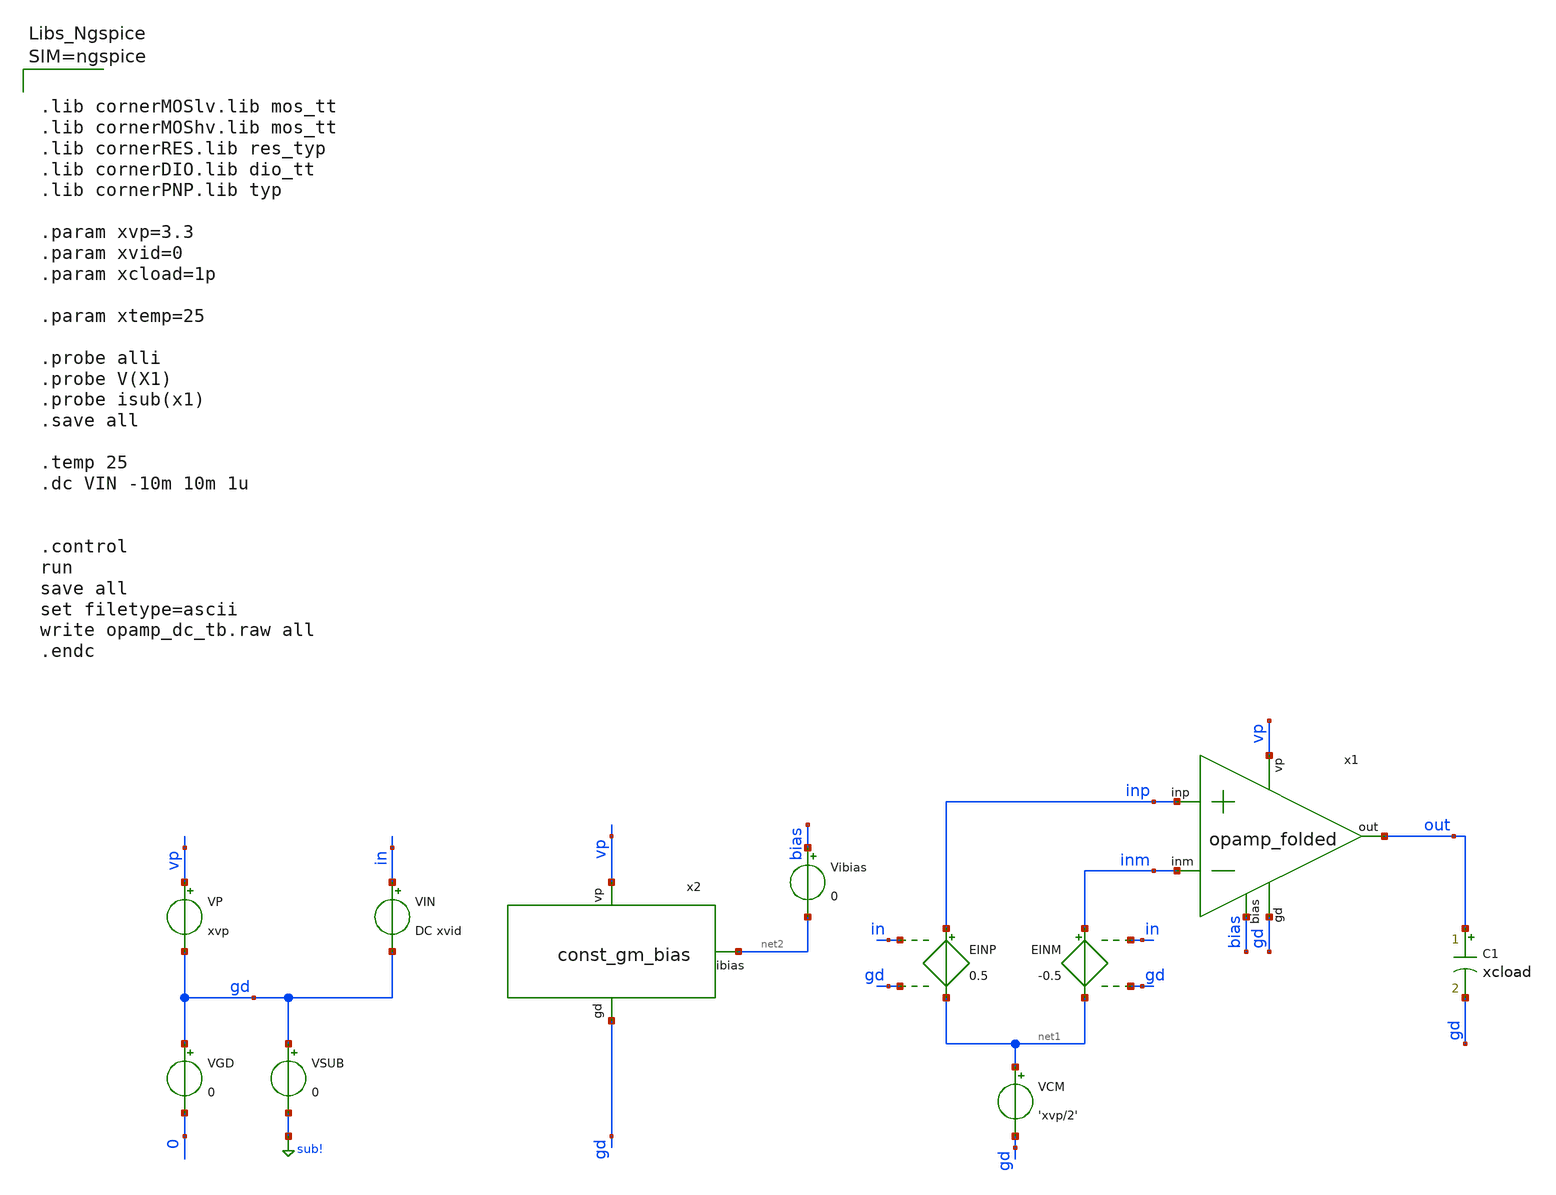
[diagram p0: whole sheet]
** sch_path: bandgap_res_tb/opamp_dc_tb.sch
**.subckt opamp_dc_tb
EINP inp net1 in gd 0.5
EINM inm net1 in gd -0.5
C1 out gd xcload m=1
VGD gd 0 0
VP vp gd xvp
VSUB gd sub! 0
VIN in gd DC xvid
VCM net1 gd 'xvp/2'
Vibias bias net2 0
.save i(vibias)
x1 vp inp inm out bias gd opamp_folded
x2 vp net2 gd const_gm_bias
**** begin user architecture code



.lib cornerMOSlv.lib mos_tt
.lib cornerMOShv.lib mos_tt
.lib cornerRES.lib res_typ
.lib cornerDIO.lib dio_tt
.lib cornerPNP.lib typ

.param xvp=3.3
.param xvid=0
.param xcload=1p

.param xtemp=25

.probe alli
.probe V(X1)
.probe isub(x1)
.save all

.temp 25
.dc VIN -10m 10m 1u


.control
run
save all
set filetype=ascii
write opamp_dc_tb.raw all
.endc



**** end user architecture code
**.ends

* expanding   symbol:  /foss/designs/master/bandgap_res/opamp_folded.sym # of pins=6
** sym_path: /foss/designs/master/bandgap_res/opamp_folded.sym
** sch_path: /foss/designs/master/bandgap_res/opamp_folded.sch
.subckt opamp_folded vp inp inm out bias gd
*.ipin bias
*.opin out
*.ipin vp
*.ipin inp
*.ipin inm
*.ipin gd
XM1 inp_fold inp net1 gd sg13_hv_nmos w=1.2u l=0.9u ng=1 m=4 mm_ok=1
XM2 inm_fold inm net1 gd sg13_hv_nmos w=1.2u l=0.9u ng=1 m=4 mm_ok=1
XM3 tele_p tele_g gd gd sg13_hv_nmos w=1.2u l=0.9u ng=1 m=2 mm_ok=1
XM4 tele_m tele_g gd gd sg13_hv_nmos w=1.2u l=0.9u ng=1 m=2 mm_ok=1
XM5 tele_g bias2 tele_p gd sg13_hv_nmos w=1.2u l=0.9u ng=1 m=2 mm_ok=1
XM6 out bias2 tele_m gd sg13_hv_nmos w=1.2u l=0.9u ng=1 m=2 mm_ok=1
XM7 tele_g bias3 inp_fold vp sg13_hv_pmos w=3.6u l=0.9u ng=1 m=2 mm_ok=1
XM8 out bias3 inm_fold vp sg13_hv_pmos w=3.6u l=0.9u ng=1 m=2 mm_ok=1
XM9 inp_fold bias4 vp vp sg13_hv_pmos w=3.6u l=0.9u ng=1 m=4 mm_ok=1
XM10 inm_fold bias4 vp vp sg13_hv_pmos w=3.6u l=0.9u ng=1 m=4 mm_ok=1
XM11 net1 bias gd gd sg13_hv_nmos w=1.2u l=0.9u ng=1 m=4 mm_ok=1
XM12 bias bias gd gd sg13_hv_nmos w=1.2u l=0.9u ng=1 m=2 mm_ok=1
XM13 bias4 bias gd gd sg13_hv_nmos w=1.2u l=0.9u ng=1 m=2 mm_ok=1
XM14 bias4 bias4 vp vp sg13_hv_pmos w=3.6u l=0.9u ng=1 m=2 mm_ok=1
XM15 bias3 bias gd gd sg13_hv_nmos w=1.2u l=0.9u ng=1 m=2 mm_ok=1
XM16 bias3 bias3 net3 vp sg13_hv_pmos w=3.6u l=0.9u ng=1 m=1 mm_ok=1
XM17 net3 bias3 vp vp sg13_hv_pmos w=3.6u l=0.9u ng=1 m=1 mm_ok=1
XM18 net2 bias2 gd gd sg13_hv_nmos w=1.2u l=0.9u ng=1 m=1 mm_ok=1
XM19 bias2 bias2 net2 gd sg13_hv_nmos w=1.2u l=0.9u ng=1 m=1 mm_ok=1
XM20 bias2 bias4 vp vp sg13_hv_pmos w=3.6u l=0.9u ng=1 m=4 mm_ok=1
.ends


* expanding   symbol:  /foss/designs/master/bandgap_res/const_gm_bias.sym # of pins=3
** sym_path: bandgap_res/const_gm_bias.sym
** sch_path: bandgap_res/const_gm_bias.sch
.subckt const_gm_bias vp ibias gd
*.ipin vp
*.ipin gd
*.opin ibias
XM1 net1 nbias gd gd sg13_hv_nmos w=0.6u l=2u ng=1 m=1 mm_ok=1
XM3 net2 nbias vr gd sg13_hv_nmos w=0.6u l=2u ng=1 m=4 mm_ok=1
XM7 pbias pbias net3 vp sg13_hv_pmos w=0.6u l=2u ng=1 m=1 mm_ok=1
XM5 nbias pbias net4 vp sg13_hv_pmos w=0.6u l=2u ng=1 m=1 mm_ok=1
XM2 nbias nbias net1 gd sg13_hv_nmos w=0.6u l=2u ng=1 m=1 mm_ok=1
XM4 pbias nbias net2 gd sg13_hv_nmos w=0.6u l=2u ng=1 m=4 mm_ok=1
XM8 net3 pbias vp vp sg13_hv_pmos w=0.6u l=2u ng=1 m=1 mm_ok=1
XM6 net4 pbias vp vp sg13_hv_pmos w=0.6u l=2u ng=1 m=1 mm_ok=1
XM9 ibias pbias net5 vp sg13_hv_pmos w=0.6u l=2u ng=1 m=1 mm_ok=1
XM10 net5 pbias vp vp sg13_hv_pmos w=0.6u l=2u ng=1 m=1 mm_ok=1
XRbias vr gd sub! rhigh w=0.5e-6 l=0.96e-6 m=1 b=5 mm_ok=1
.ends

.GLOBAL sub!
.end
